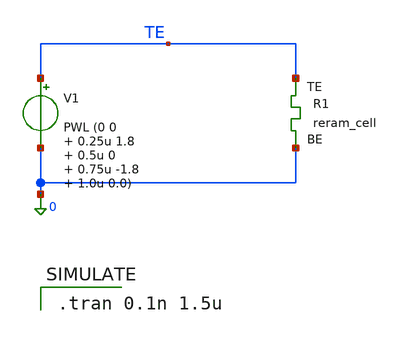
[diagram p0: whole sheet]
** sch_path: extern/rram_model/xschem/reram_examples/reram_example_ngspice.sch
**.subckt reram_example_ngspice
V1 TE 0 PWL (0 0 0.25u 1.8 0.5u 0 0.75u -1.8 1.0u 0.0)
XR1 TE 0 sky130_fd_pr_reram__reram_cell Tfilament_0=3.3e-9
**** begin user architecture code

.tran 0.1n 1.5u


** opencircuitdesign pdks install
.include $PDK_ROOT/open_pdks/sky130/sky130B/libs.tech/combined/skywater-pdk-libs-sky130_fd_pr_reram/cells/reram_cell/sky130_fd_pr_reram__reram_cell.spice


.control
save all
run
write reram_example_ngspice.raw
.endc



**** end user architecture code
**.ends
.end
